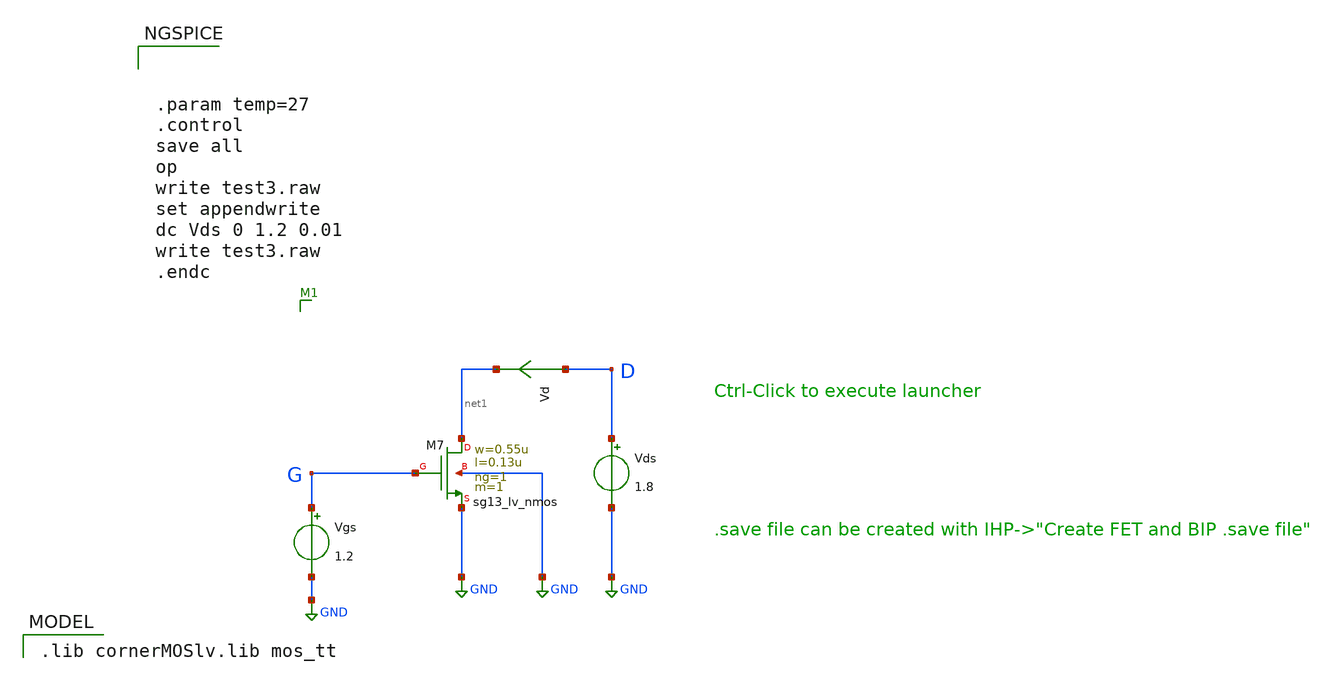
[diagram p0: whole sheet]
** sch_path: schematic/test3.sch
**.subckt test3
Vgs G GND 1.2
Vds D GND 1.8
Vd D net1 0
.save i(vd)
XM7 net1 G GND GND sg13_lv_nmos w=0.55u l=0.13u ng=1 m=1 mm_ok=1
**** begin user architecture code
 .lib cornerMOSlv.lib mos_tt




.param temp=27
.control
save all
op
write test3.raw
set appendwrite
dc Vds 0 1.2 0.01
write test3.raw
.endc


**** end user architecture code
**.ends
.GLOBAL GND
.end
